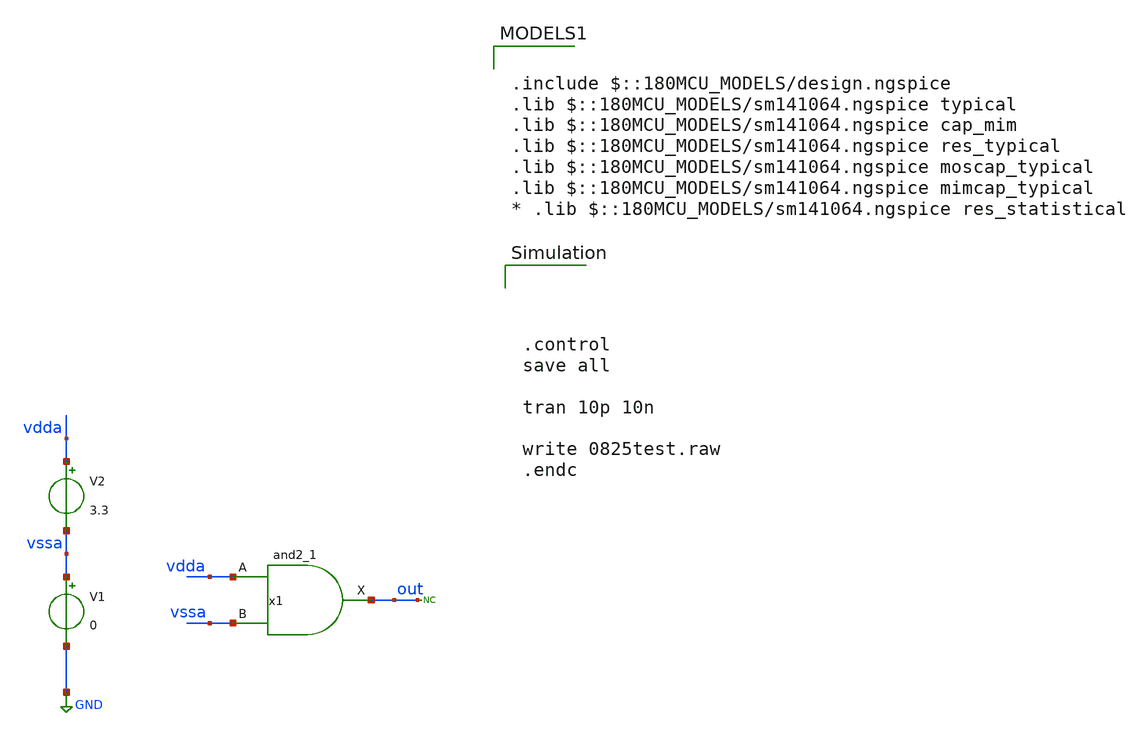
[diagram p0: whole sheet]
** sch_path: designs/libs/qw_core_analog/0825test.sch
**.subckt 0825test
x1 vdda vssa VSSd VDDd VSSd VDDd out gf180mcu_fd_sc_mcu9t5v0__and2_1
V1 vssa GND 0
V2 vdda vssa 3.3
* noconn out
**** begin user architecture code




.control
save all

tran 10p 10n

write 0825test.raw
.endc



.include $::180MCU_MODELS/design.ngspice
.lib $::180MCU_MODELS/sm141064.ngspice typical
.lib $::180MCU_MODELS/sm141064.ngspice cap_mim
.lib $::180MCU_MODELS/sm141064.ngspice res_typical
.lib $::180MCU_MODELS/sm141064.ngspice moscap_typical
.lib $::180MCU_MODELS/sm141064.ngspice mimcap_typical
* .lib $::180MCU_MODELS/sm141064.ngspice res_statistical

**** end user architecture code
**.ends
.GLOBAL GND
.end
